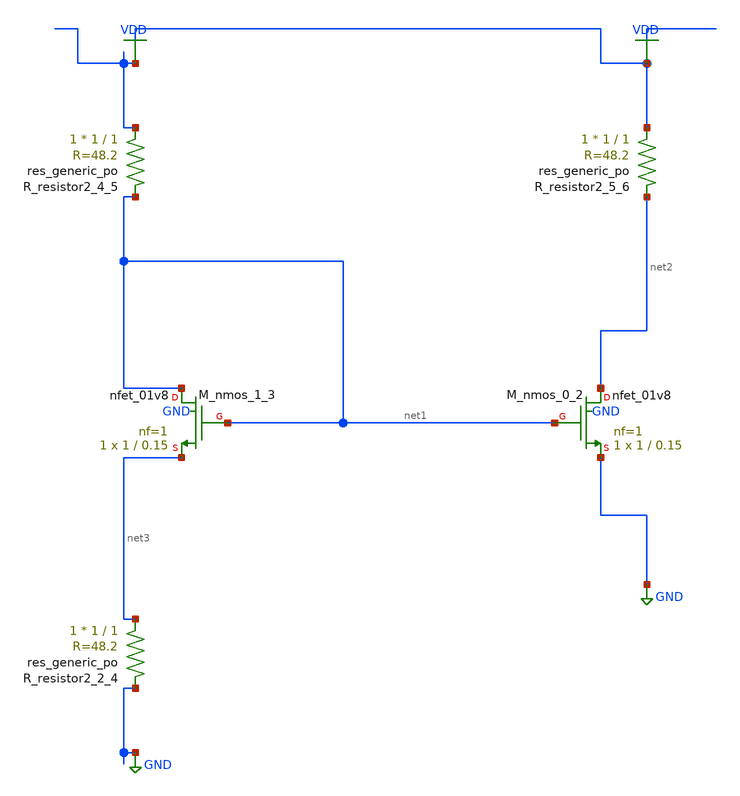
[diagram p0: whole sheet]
** sch_path: schematics/AMSNet/324.sch
**.subckt 324
XM_nmos_0_2 net2 net1 GND GND sky130_fd_pr__nfet_01v8 L=0.15 W=1 nf=1 ad='int((1 + 1)/2) * 1 / 1 * 0.29'
+ as='int((1 + 2)/2) * 1 / 1 * 0.29' pd='2*int((1 + 1)/2) * (1 / 1 + 0.29)' ps='2*int((1 + 2)/2) * (1 / 1 + 0.29)'
+ nrd='0.29 / 1 ' nrs='0.29 / 1 ' sa=0 sb=0 sd=0 mult=1 m=1
XM_nmos_1_3 net1 net1 net3 GND sky130_fd_pr__nfet_01v8 L=0.15 W=1 nf=1 ad='int((1 + 1)/2) * 1 / 1 * 0.29'
+ as='int((1 + 2)/2) * 1 / 1 * 0.29' pd='2*int((1 + 1)/2) * (1 / 1 + 0.29)' ps='2*int((1 + 2)/2) * (1 / 1 + 0.29)'
+ nrd='0.29 / 1 ' nrs='0.29 / 1 ' sa=0 sb=0 sd=0 mult=1 m=1
XR_resistor2_2_4 net3 GND sky130_fd_pr__res_generic_po W=1 L=1 m=1
XR_resistor2_4_5 VDD net1 sky130_fd_pr__res_generic_po W=1 L=1 m=1
XR_resistor2_5_6 VDD net2 sky130_fd_pr__res_generic_po W=1 L=1 m=1
**.ends
.GLOBAL GND
.GLOBAL VDD
.end
